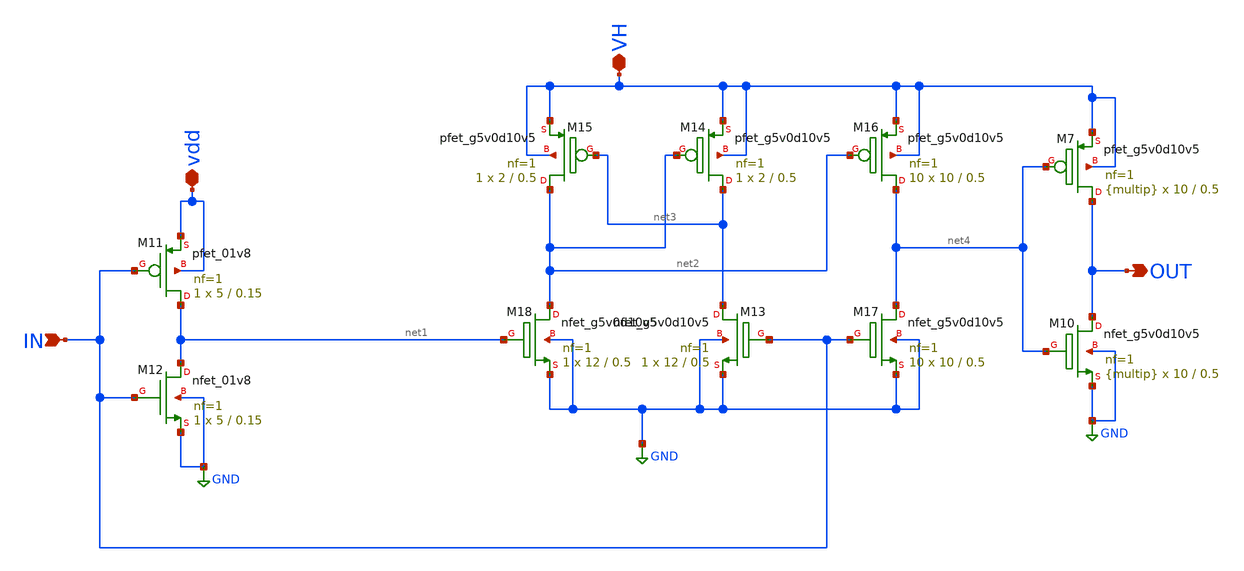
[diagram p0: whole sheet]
** sch_path: xschem/dev_switches/DCDC_5V_FINAL/LS_FINAL.sch
**.subckt LS_FINAL IN vdd VH OUT
*.ipin IN
*.iopin vdd
*.iopin VH
*.opin OUT
XM11 net1 IN vdd vdd sky130_fd_pr__pfet_01v8 L=0.15 W=5 nf=1 ad='int((nf+1)/2) * W/nf * 0.29' as='int((nf+2)/2) * W/nf * 0.29'
+ pd='2*int((nf+1)/2) * (W/nf + 0.29)' ps='2*int((nf+2)/2) * (W/nf + 0.29)' nrd='0.29 / W' nrs='0.29 / W'
+ sa=0 sb=0 sd=0 mult=1 m=1
XM12 net1 IN GND GND sky130_fd_pr__nfet_01v8 L=0.15 W=5 nf=1 ad='int((nf+1)/2) * W/nf * 0.29' as='int((nf+2)/2) * W/nf * 0.29'
+ pd='2*int((nf+1)/2) * (W/nf + 0.29)' ps='2*int((nf+2)/2) * (W/nf + 0.29)' nrd='0.29 / W' nrs='0.29 / W'
+ sa=0 sb=0 sd=0 mult=1 m=1
XM15 net2 net3 VH VH sky130_fd_pr__pfet_g5v0d10v5 L=0.5 W=2 nf=1 ad='int((nf+1)/2) * W/nf * 0.29' as='int((nf+2)/2) * W/nf * 0.29'
+ pd='2*int((nf+1)/2) * (W/nf + 0.29)' ps='2*int((nf+2)/2) * (W/nf + 0.29)' nrd='0.29 / W' nrs='0.29 / W'
+ sa=0 sb=0 sd=0 mult=1 m=1
XM14 net3 net2 VH VH sky130_fd_pr__pfet_g5v0d10v5 L=0.5 W=2 nf=1 ad='int((nf+1)/2) * W/nf * 0.29' as='int((nf+2)/2) * W/nf * 0.29'
+ pd='2*int((nf+1)/2) * (W/nf + 0.29)' ps='2*int((nf+2)/2) * (W/nf + 0.29)' nrd='0.29 / W' nrs='0.29 / W'
+ sa=0 sb=0 sd=0 mult=1 m=1
XM16 net4 net2 VH VH sky130_fd_pr__pfet_g5v0d10v5 L=0.5 W=10 nf=1 ad='int((nf+1)/2) * W/nf * 0.29' as='int((nf+2)/2) * W/nf * 0.29'
+ pd='2*int((nf+1)/2) * (W/nf + 0.29)' ps='2*int((nf+2)/2) * (W/nf + 0.29)' nrd='0.29 / W' nrs='0.29 / W'
+ sa=0 sb=0 sd=0 mult=10 m=10
XM18 net2 net1 GND GND sky130_fd_pr__nfet_g5v0d10v5 L=0.5 W=12 nf=1 ad='int((nf+1)/2) * W/nf * 0.29'
+ as='int((nf+2)/2) * W/nf * 0.29' pd='2*int((nf+1)/2) * (W/nf + 0.29)' ps='2*int((nf+2)/2) * (W/nf + 0.29)'
+ nrd='0.29 / W' nrs='0.29 / W' sa=0 sb=0 sd=0 mult=1 m=1
XM13 net3 IN GND GND sky130_fd_pr__nfet_g5v0d10v5 L=0.5 W=12 nf=1 ad='int((nf+1)/2) * W/nf * 0.29' as='int((nf+2)/2) * W/nf * 0.29'
+ pd='2*int((nf+1)/2) * (W/nf + 0.29)' ps='2*int((nf+2)/2) * (W/nf + 0.29)' nrd='0.29 / W' nrs='0.29 / W'
+ sa=0 sb=0 sd=0 mult=1 m=1
XM17 net4 IN GND GND sky130_fd_pr__nfet_g5v0d10v5 L=0.5 W=10 nf=1 ad='int((nf+1)/2) * W/nf * 0.29' as='int((nf+2)/2) * W/nf * 0.29'
+ pd='2*int((nf+1)/2) * (W/nf + 0.29)' ps='2*int((nf+2)/2) * (W/nf + 0.29)' nrd='0.29 / W' nrs='0.29 / W'
+ sa=0 sb=0 sd=0 mult=10 m=10
XM7 OUT net4 VH VH sky130_fd_pr__pfet_g5v0d10v5 L=0.5 W=10 nf=1 ad='int((nf+1)/2) * W/nf * 0.29' as='int((nf+2)/2) * W/nf * 0.29'
+ pd='2*int((nf+1)/2) * (W/nf + 0.29)' ps='2*int((nf+2)/2) * (W/nf + 0.29)' nrd='0.29 / W' nrs='0.29 / W'
+ sa=0 sb=0 sd=0 mult={multip} m={multip}
XM10 OUT net4 GND GND sky130_fd_pr__nfet_g5v0d10v5 L=0.5 W=10 nf=1 ad='int((nf+1)/2) * W/nf * 0.29' as='int((nf+2)/2) * W/nf * 0.29'
+ pd='2*int((nf+1)/2) * (W/nf + 0.29)' ps='2*int((nf+2)/2) * (W/nf + 0.29)' nrd='0.29 / W' nrs='0.29 / W'
+ sa=0 sb=0 sd=0 mult={multip} m={multip}
**** begin user architecture code

*
* Parameters

*.PARAM BAT=1.8
.PARAM W12=12 W45=2 LLS=0.5 multip=40
*.option scale=1e-6
*.options TEMP = 65.0

* Models
*.lib /foss/pdk/sky130A/libs.tech/ngspice/sky130.lib.spice TT

*Fuentes******
*VBAT VDD 0 DC BAT
*VHIGH VH 0 DC 5
*vin IN 0 dc 0 PULSE (0 BAT .1n .1n .1n 10n 20n)

*COUT OUT 0 20p


*.options savecurrents
*.save all
*+ @M.XM12.msky130_fd_pr_nfet_01v8[id]

*.control
*tran 0.1n 100n
*plot v(IN) v(LS1) v(OUT) v(net6) i(@M.XM12.msky130_fd_pr_nfet_01v8[id])
*write LS_FINAL.raw
*.endc
*.end
*

**** end user architecture code
**.ends
.GLOBAL GND
.end
